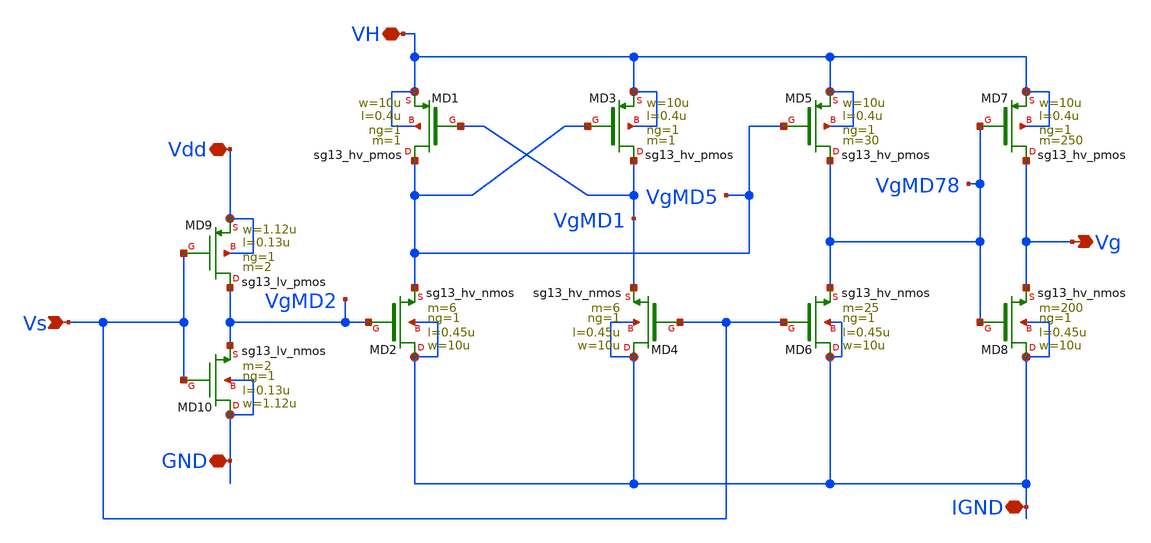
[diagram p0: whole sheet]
** sch_path: xschem/GD/GD_vto1p1.sch
**.subckt GD_vto1p1 VH Vdd Vs Vg GND IGND
*.iopin VH
*.iopin Vdd
*.ipin Vs
*.opin Vg
*.iopin GND
*.iopin IGND
XMD9 VgMD2 Vs Vdd Vdd sg13_lv_pmos w=1.12u l=0.13u ng=1 m=2 mm_ok=1
XMD10 GND Vs VgMD2 GND sg13_lv_nmos w=1.12u l=0.13u ng=1 m=2 mm_ok=1
XMD1 VgMD5 VgMD1 VH VH sg13_hv_pmos w=10u l=0.4u ng=1 m=1 mm_ok=1
XMD3 VgMD1 VgMD5 VH VH sg13_hv_pmos w=10u l=0.4u ng=1 m=1 mm_ok=1
XMD5 VgMD78 VgMD5 VH VH sg13_hv_pmos w=10u l=0.4u ng=1 m=30 mm_ok=1
XMD7 Vg VgMD78 VH VH sg13_hv_pmos w=10u l=0.4u ng=1 m=250 mm_ok=1
XMD2 IGND VgMD2 VgMD5 IGND sg13_hv_nmos w=10u l=0.45u ng=1 m=6 mm_ok=1
XMD4 IGND Vs VgMD1 IGND sg13_hv_nmos w=10u l=0.45u ng=1 m=6 mm_ok=1
XMD6 IGND Vs VgMD78 IGND sg13_hv_nmos w=10u l=0.45u ng=1 m=25 mm_ok=1
XMD8 IGND VgMD78 Vg IGND sg13_hv_nmos w=10u l=0.45u ng=1 m=200 mm_ok=1
**.ends
.end
